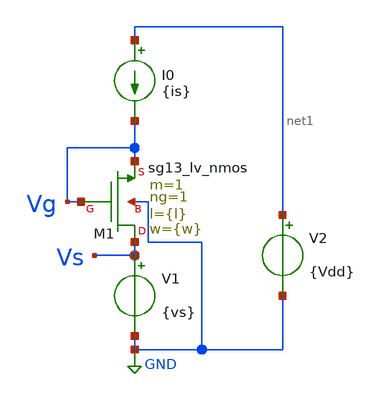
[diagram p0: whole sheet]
** sch_path: Parametros_Psp/n_test.sch
**.subckt n_test
V1 Vs GND {vs}
V2 net1 GND {Vdd}
XM1 Vs Vg Vg GND sg13_lv_nmos w={w} l={l} ng=1 m=1 mm_ok=1
I0 net1 Vg {is}
**** begin user architecture code


* Circuit Parameters
.param vs = 3
.param step = 0.01
.param Vdd = 1.8
.param is = 0.173u
.param w = 5.0u
.param l = 0.18u
* Include Models
.lib /opt/pdks/ihp-sg13g2/libs.tech/ngspice/models/cornerMOSlv.lib mos_tt
.lib /opt/pdks/ihp-sg13g2/libs.tech/ngspice/models/cornerMOShv.lib mos_tt
* OP Parameters & Singals to save
.save all
*Simulations
.dc V1 -1 {vs} {step}
.control
run
setplot dc1
plot v(Vg)
set filetype = ascii
write dcsweep.raw
.endc
.end


**** end user architecture code
**.ends
.GLOBAL GND
.end
